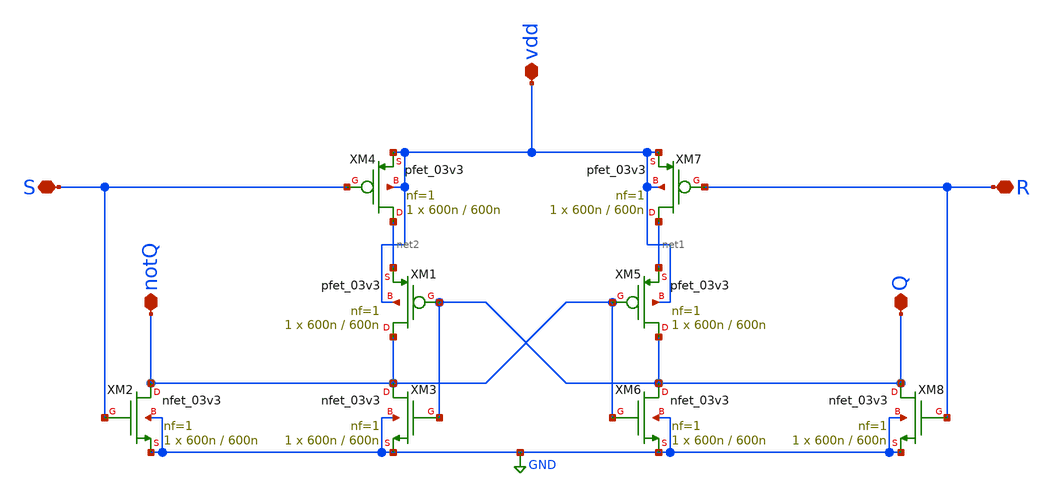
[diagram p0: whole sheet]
** sch_path: Clock_Reference/symbols_clock/RS.sch
**.subckt RS R S vdd notQ Q
*.iopin R
*.iopin S
*.iopin vdd
*.iopin notQ
*.iopin Q
XM1 notQ Q net2 vdd pfet_03v3 L=600n W=600n nf=1 ad='int((nf+1)/2) * W/nf * 0.18u' as='int((nf+2)/2) * W/nf * 0.18u'
+ pd='2*int((nf+1)/2) * (W/nf + 0.18u)' ps='2*int((nf+2)/2) * (W/nf + 0.18u)' nrd='0.18u / W' nrs='0.18u / W'
+ sa=0 sb=0 sd=0 m=1
XM2 notQ S GND GND nfet_03v3 L=600n W=600n nf=1 ad='int((nf+1)/2) * W/nf * 0.18u' as='int((nf+2)/2) * W/nf * 0.18u'
+ pd='2*int((nf+1)/2) * (W/nf + 0.18u)' ps='2*int((nf+2)/2) * (W/nf + 0.18u)' nrd='0.18u / W' nrs='0.18u / W'
+ sa=0 sb=0 sd=0 m=1
XM3 notQ Q GND GND nfet_03v3 L=600n W=600n nf=1 ad='int((nf+1)/2) * W/nf * 0.18u' as='int((nf+2)/2) * W/nf * 0.18u'
+ pd='2*int((nf+1)/2) * (W/nf + 0.18u)' ps='2*int((nf+2)/2) * (W/nf + 0.18u)' nrd='0.18u / W' nrs='0.18u / W'
+ sa=0 sb=0 sd=0 m=1
XM4 net2 S vdd vdd pfet_03v3 L=600n W=600n nf=1 ad='int((nf+1)/2) * W/nf * 0.18u' as='int((nf+2)/2) * W/nf * 0.18u'
+ pd='2*int((nf+1)/2) * (W/nf + 0.18u)' ps='2*int((nf+2)/2) * (W/nf + 0.18u)' nrd='0.18u / W' nrs='0.18u / W'
+ sa=0 sb=0 sd=0 m=1
XM5 Q notQ net1 vdd pfet_03v3 L=600n W=600n nf=1 ad='int((nf+1)/2) * W/nf * 0.18u' as='int((nf+2)/2) * W/nf * 0.18u'
+ pd='2*int((nf+1)/2) * (W/nf + 0.18u)' ps='2*int((nf+2)/2) * (W/nf + 0.18u)' nrd='0.18u / W' nrs='0.18u / W'
+ sa=0 sb=0 sd=0 m=1
XM6 Q notQ GND GND nfet_03v3 L=600n W=600n nf=1 ad='int((nf+1)/2) * W/nf * 0.18u' as='int((nf+2)/2) * W/nf * 0.18u'
+ pd='2*int((nf+1)/2) * (W/nf + 0.18u)' ps='2*int((nf+2)/2) * (W/nf + 0.18u)' nrd='0.18u / W' nrs='0.18u / W'
+ sa=0 sb=0 sd=0 m=1
XM7 net1 R vdd vdd pfet_03v3 L=600n W=600n nf=1 ad='int((nf+1)/2) * W/nf * 0.18u' as='int((nf+2)/2) * W/nf * 0.18u'
+ pd='2*int((nf+1)/2) * (W/nf + 0.18u)' ps='2*int((nf+2)/2) * (W/nf + 0.18u)' nrd='0.18u / W' nrs='0.18u / W'
+ sa=0 sb=0 sd=0 m=1
XM8 Q R GND GND nfet_03v3 L=600n W=600n nf=1 ad='int((nf+1)/2) * W/nf * 0.18u' as='int((nf+2)/2) * W/nf * 0.18u'
+ pd='2*int((nf+1)/2) * (W/nf + 0.18u)' ps='2*int((nf+2)/2) * (W/nf + 0.18u)' nrd='0.18u / W' nrs='0.18u / W'
+ sa=0 sb=0 sd=0 m=1
**.ends
.GLOBAL GND
.end
